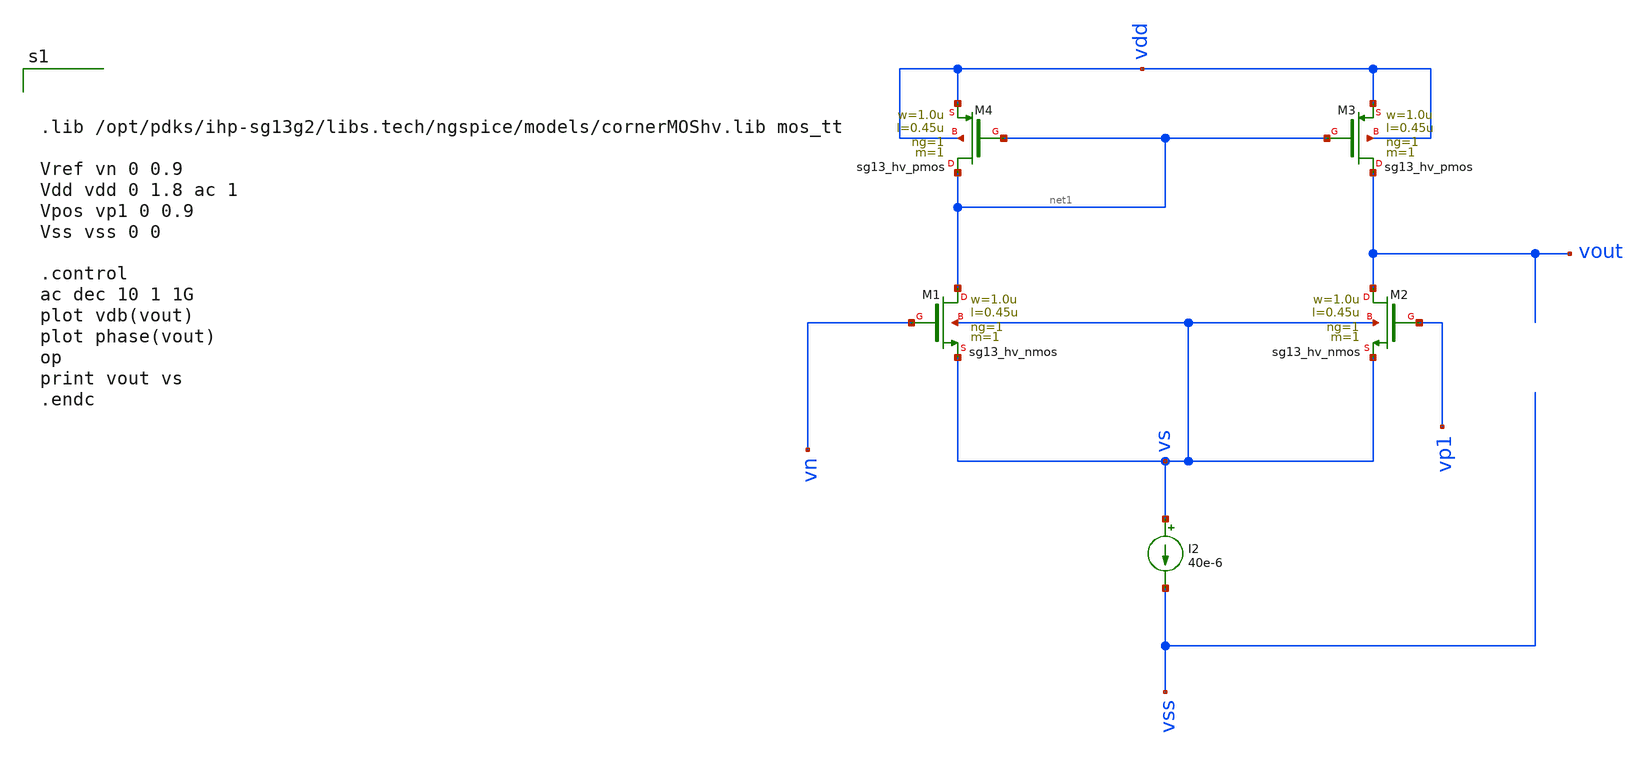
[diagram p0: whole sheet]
** sch_path: test-python/sstadex/xschem/ota_tb_ihp.sch
**.subckt ota_tb_ihp
I2 vs vss 40e-6
XM1 net1 vn vs vs sg13_hv_nmos w=1.0u l=0.45u ng=1 m=1 mm_ok=1
XM2 vout vp1 vs vs sg13_hv_nmos w=1.0u l=0.45u ng=1 m=1 mm_ok=1
XM3 vout net1 vdd vdd sg13_hv_pmos w=1.0u l=0.45u ng=1 m=1 mm_ok=1
XM4 net1 net1 vdd vdd sg13_hv_pmos w=1.0u l=0.45u ng=1 m=1 mm_ok=1
**** begin user architecture code



.lib /opt/pdks/ihp-sg13g2/libs.tech/ngspice/models/cornerMOShv.lib mos_tt

Vref vn 0 0.9
Vdd vdd 0 1.8 ac 1
Vpos vp1 0 0.9
Vss vss 0 0

.control
ac dec 10 1 1G
plot vdb(vout)
plot phase(vout)
op
print vout vs
.endc



**** end user architecture code
**.ends
.end
